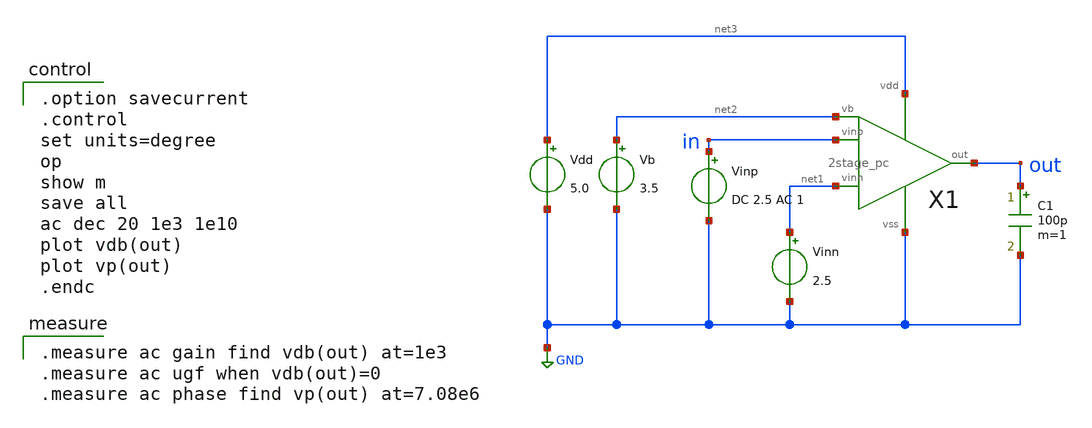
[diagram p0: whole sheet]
** sch_path: member_project/opamp/makoto645/testbench/2stage_pc_ac.sch
**.subckt 2stage_pc_ac
Vdd net3 GND 5.0
Vb net2 GND 3.5
Vinn net1 GND 2.5
Vinp in GND DC 2.5 AC 1
C1 out GND 100p m=1
X1 in net1 net2 out net3 GND 2stage_pc
**** begin user architecture code

.option savecurrent
.control
set units=degree
op
show m
save all
ac dec 20 1e3 1e10
plot vdb(out)
plot vp(out)
.endc


.measure ac gain find vdb(out) at=1e3
.measure ac ugf when vdb(out)=0
.measure ac phase find vp(out) at=7.08e6

 .include $::LIB/ip62_models
**** end user architecture code
**.ends

* expanding   symbol:  2stage_pc.sym # of pins=6
** sym_path: 2stage_pc.sym
** sch_path: 2stage_pc.sch
.subckt 2stage_pc vinp vinn vb out vdd vss
*.ipin vinp
*.ipin vinn
*.ipin vb
*.opin out
*.iopin vdd
*.iopin vss
X1 vinp vinn net2 vdd vss vb diff
X2 net2 vb out vdd vss cs
XM6 net1 vb vdd vdd PMOS w=48u l=2u as=0 ad=0 ps=0 pd=0 nrd=0 nrs=0 m=1
XM1 net1 net1 net3 vss NMOS w=22u l=2u as=0 ad=0 ps=0 pd=0 nrd=0 nrs=0 m=1
XM7 net3 net3 vss vss NMOS w=22u l=2u as=0 ad=0 ps=0 pd=0 nrd=0 nrs=0 m=1
XM2 net4 net1 net2 vss NMOS w=40u l=2u as=0 ad=0 ps=0 pd=0 nrd=0 nrs=0 m=1
XXC1 net4 out vss F_CSIO c=8.64p x=120u y=120u m=1
.ends


* expanding   symbol:  diff.sym # of pins=6
** sym_path: diff.sym
** sch_path: diff.sch
.subckt diff vinp vinn out vdd vss vb
*.ipin vinn
*.ipin vinp
*.ipin vb
*.opin out
*.iopin vdd
*.iopin vss
XM5 net2 vb vdd vdd PMOS w=200u l=2u as=0 ad=0 ps=0 pd=0 nrd=0 nrs=0 m=1
XM1 net1 vinn net2 net2 PMOS w=100u l=2u as=0 ad=0 ps=0 pd=0 nrd=0 nrs=0 m=1
XM2 out vinp net2 net2 PMOS w=100u l=2u as=0 ad=0 ps=0 pd=0 nrd=0 nrs=0 m=1
XM3 net1 net1 vss vss NMOS w=50u l=2u as=0 ad=0 ps=0 pd=0 nrd=0 nrs=0 m=1
XM4 out net1 vss vss NMOS w=50u l=2u as=0 ad=0 ps=0 pd=0 nrd=0 nrs=0 m=1
.ends


* expanding   symbol:  cs.sym # of pins=5
** sym_path: cs.sym
** sch_path: cs.sch
.subckt cs vin vb out vdd vss
*.ipin vb
*.ipin vin
*.opin out
*.iopin vss
*.iopin vdd
XM6 out vb vdd vdd PMOS w=480u l=2u as=0 ad=0 ps=0 pd=0 nrd=0 nrs=0 m=1
XM7 out vin vss vss NMOS w=220u l=2u as=0 ad=0 ps=0 pd=0 nrd=0 nrs=0 m=1
.ends

.GLOBAL GND
.end
